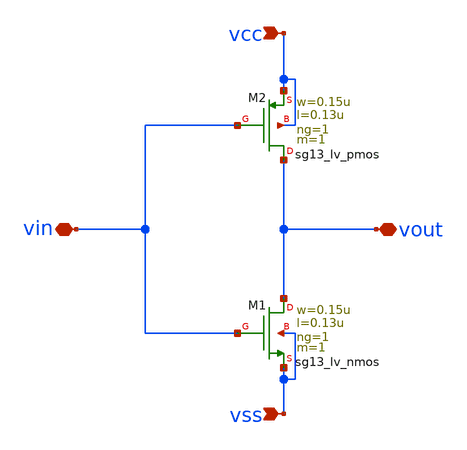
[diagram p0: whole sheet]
** sch_path: 001_Inverter/Inverter.sch
**.subckt Inverter vin vout vcc vss
*.iopin vin
*.iopin vout
*.ipin vcc
*.ipin vss
XM1 vout vin vss vss sg13_lv_nmos w=0.15u l=0.13u ng=1 m=1 mm_ok=1
XM2 vout vin vcc vcc sg13_lv_pmos w=0.15u l=0.13u ng=1 m=1 mm_ok=1
**.ends
.end
